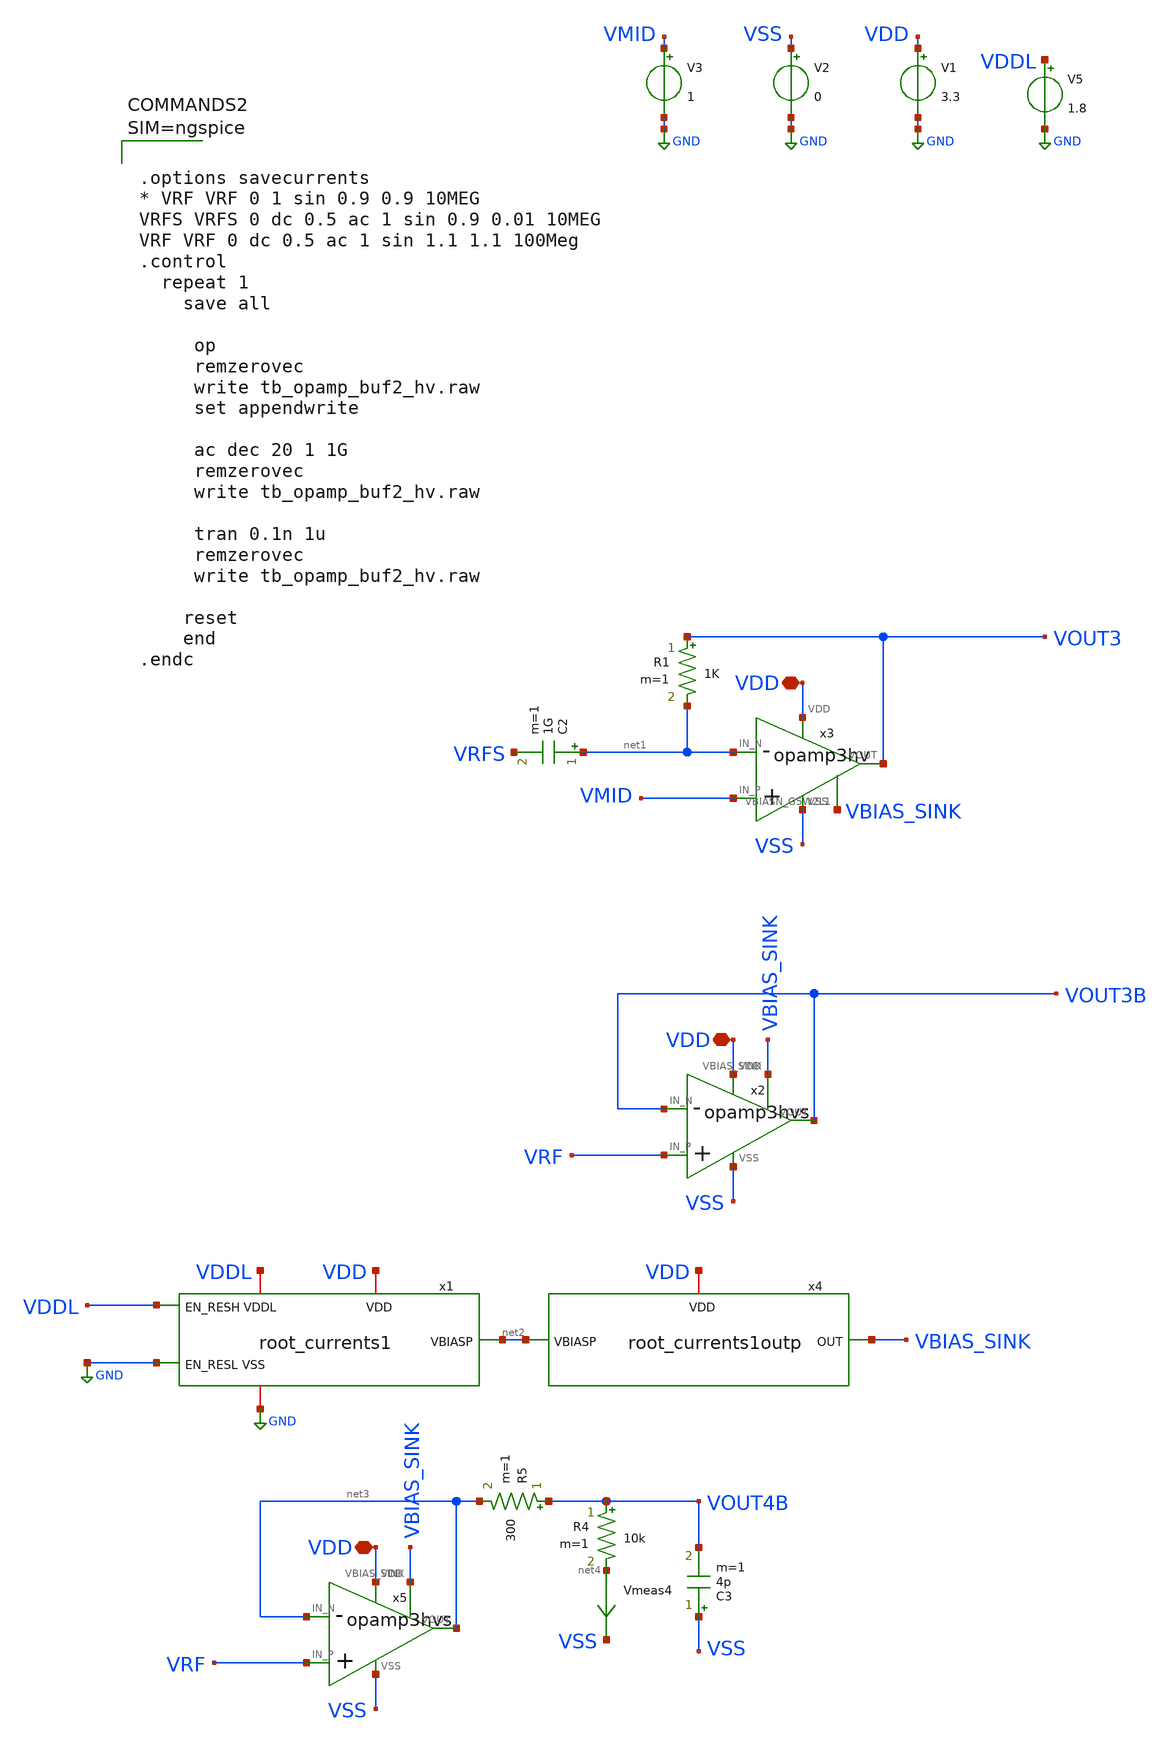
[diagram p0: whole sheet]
** sch_path: xschem/tb_opamp_buf2_hv.sch
**.subckt tb_opamp_buf2_hv VDD VDD VDD
*.iopin VDD
*.iopin VDD
*.iopin VDD
V1 VDD GND 3.3
V2 VSS GND 0
x3 net1 VMID VOUT3 VBIAS_SINK VDD VSS opamp3hv
V3 VMID GND 1
C2 net1 VRFS 1G m=1
R1 VOUT3 net1 1K m=1
x2 VOUT3B VRF VOUT3B VDD VSS VBIAS_SINK opamp3hvs
x1 VDDL GND net2 VDD VDDL GND root_currents1
x4 net2 VBIAS_SINK VDD root_currents1outp
V5 VDDL GND 1.8
x5 net3 VRF net3 VDD VSS VBIAS_SINK opamp3hvs
R4 VOUT4B net4 10k m=1
Vmeas4 net4 VSS 0
.save i(vmeas4)
C3 VSS VOUT4B 4p m=1
R5 VOUT4B net3 300 m=1
**** begin user architecture code

** opencircuitdesign pdks install
.lib $::SKYWATER_MODELS/sky130.lib.spice tt





.options savecurrents
* VRF VRF 0 1 sin 0.9 0.9 10MEG
VRFS VRFS 0 dc 0.5 ac 1 sin 0.9 0.01 10MEG
VRF VRF 0 dc 0.5 ac 1 sin 1.1 1.1 100Meg
.control
  repeat 1
    save all

     op
     remzerovec
     write tb_opamp_buf2_hv.raw
     set appendwrite

     ac dec 20 1 1G
     remzerovec
     write tb_opamp_buf2_hv.raw

     tran 0.1n 1u
     remzerovec
     write tb_opamp_buf2_hv.raw

    reset
    end
.endc



**** end user architecture code
**.ends

* expanding   symbol:  opamp3hv.sym # of pins=6
** sym_path: xschem/opamp3hv.sym
** sch_path: xschem/opamp3hv.sch
.subckt opamp3hv IN_N IN_P VOUT VBIASN_G5W2L1 VDD VSS
*.iopin VDD
*.iopin VSS
*.ipin IN_N
*.opin VOUT
*.ipin IN_P
*.iopin VBIASN_G5W2L1
vimeasn net2 VN 0
.save i(vimeasn)
vimeasp net3 voutstage1 0
.save i(vimeasp)
vicom vcom net1 0
.save i(vicom)
XC1 VOUT voutstage1 sky130_fd_pr__cap_mim_m3_1 W=2 L=2 MF=1 m=1
XM6 net1 VBIASN_G5W2L1 VSS VSS sky130_fd_pr__nfet_g5v0d10v5 L=1 W=2 nf=1 ad='int((nf+1)/2) * W/nf * 0.29'
+ as='int((nf+2)/2) * W/nf * 0.29' pd='2*int((nf+1)/2) * (W/nf + 0.29)' ps='2*int((nf+2)/2) * (W/nf + 0.29)'
+ nrd='0.29 / W' nrs='0.29 / W' sa=0 sb=0 sd=0 mult=1 m=1
XM8 net3 net2 VDD VDD sky130_fd_pr__pfet_g5v0d10v5 L=1 W=2 nf=1 ad='int((nf+1)/2) * W/nf * 0.29' as='int((nf+2)/2) * W/nf * 0.29'
+ pd='2*int((nf+1)/2) * (W/nf + 0.29)' ps='2*int((nf+2)/2) * (W/nf + 0.29)' nrd='0.29 / W' nrs='0.29 / W'
+ sa=0 sb=0 sd=0 mult=1 m=1
XM2 net2 net2 VDD VDD sky130_fd_pr__pfet_g5v0d10v5 L=1 W=2 nf=1 ad='int((nf+1)/2) * W/nf * 0.29' as='int((nf+2)/2) * W/nf * 0.29'
+ pd='2*int((nf+1)/2) * (W/nf + 0.29)' ps='2*int((nf+2)/2) * (W/nf + 0.29)' nrd='0.29 / W' nrs='0.29 / W'
+ sa=0 sb=0 sd=0 mult=1 m=1
XM1 VOUT voutstage1 net4 VDD sky130_fd_pr__pfet_g5v0d10v5 L=0.5 W=16 nf=1 ad='int((nf+1)/2) * W/nf * 0.29'
+ as='int((nf+2)/2) * W/nf * 0.29' pd='2*int((nf+1)/2) * (W/nf + 0.29)' ps='2*int((nf+2)/2) * (W/nf + 0.29)'
+ nrd='0.29 / W' nrs='0.29 / W' sa=0 sb=0 sd=0 mult=2 m=2
XM4 net5 VBIASN_G5W2L1 VSS VSS sky130_fd_pr__nfet_g5v0d10v5 L=0.5 W=8 nf=1 ad='int((nf+1)/2) * W/nf * 0.29'
+ as='int((nf+2)/2) * W/nf * 0.29' pd='2*int((nf+1)/2) * (W/nf + 0.29)' ps='2*int((nf+2)/2) * (W/nf + 0.29)'
+ nrd='0.29 / W' nrs='0.29 / W' sa=0 sb=0 sd=0 mult=2 m=2
XM3 VN IN_N vcom VSS sky130_fd_pr__nfet_03v3_nvt L=0.5 W=4 nf=1 ad='int((nf+1)/2) * W/nf * 0.29' as='int((nf+2)/2) * W/nf * 0.29'
+ pd='2*int((nf+1)/2) * (W/nf + 0.29)' ps='2*int((nf+2)/2) * (W/nf + 0.29)' nrd='0.29 / W' nrs='0.29 / W'
+ sa=0 sb=0 sd=0 mult=4 m=4
XM5 voutstage1 IN_P vcom VSS sky130_fd_pr__nfet_03v3_nvt L=0.5 W=4 nf=1 ad='int((nf+1)/2) * W/nf * 0.29'
+ as='int((nf+2)/2) * W/nf * 0.29' pd='2*int((nf+1)/2) * (W/nf + 0.29)' ps='2*int((nf+2)/2) * (W/nf + 0.29)'
+ nrd='0.29 / W' nrs='0.29 / W' sa=0 sb=0 sd=0 mult=4 m=4
XC2 VDD VSS sky130_fd_pr__cap_mim_m3_1 W=4 L=4 MF=1 m=1
vimeasp1 VDD net4 0
.save i(vimeasp1)
vimeasn1 VOUT net5 0
.save i(vimeasn1)
.ends


* expanding   symbol:  opamp3hvs.sym # of pins=6
** sym_path: xschem/opamp3hvs.sym
** sch_path: xschem/opamp3hvs.sch
.subckt opamp3hvs IN_N IN_P VOUT VDD VSS VBIAS_SINK
*.ipin IN_N
*.ipin IN_P
*.opin VOUT
*.iopin VDD
*.iopin VSS
*.iopin VBIAS_SINK
XM1 net1 net1 VSS VSS sky130_fd_pr__nfet_g5v0d10v5 L=0.5 W=4 nf=1 ad='int((nf+1)/2) * W/nf * 0.29' as='int((nf+2)/2) * W/nf * 0.29'
+ pd='2*int((nf+1)/2) * (W/nf + 0.29)' ps='2*int((nf+2)/2) * (W/nf + 0.29)' nrd='0.29 / W' nrs='0.29 / W'
+ sa=0 sb=0 sd=0 mult=1 m=1
vimeasn2 VBIAS_SINK net1 0
.save i(vimeasn2)
x1 IN_N IN_P VOUT net1 VDD VSS opamp3hv
.ends


* expanding   symbol:  root_currents1.sym # of pins=6
** sym_path: xschem/root_currents1.sym
** sch_path: xschem/root_currents1.sch
.subckt root_currents1 EN_RESH EN_RESL VBIASP VDD VDDL VSS
*.iopin VSS
*.ipin EN_RESH
*.opin VBIASP
*.iopin VDDL
*.iopin VDD
*.ipin EN_RESL
XR1 V1 net2 net4 sky130_fd_pr__res_high_po_0p35 L=20 mult=1 m=1
XR2 V2 net3 net5 sky130_fd_pr__res_high_po_0p69 L=8 mult=1 m=1
XM4 VMID VMID VSS VSS sky130_fd_pr__nfet_01v8_lvt L=0.5 W=4 nf=1 ad='int((nf+1)/2) * W/nf * 0.29' as='int((nf+2)/2) * W/nf * 0.29'
+ pd='2*int((nf+1)/2) * (W/nf + 0.29)' ps='2*int((nf+2)/2) * (W/nf + 0.29)' nrd='0.29 / W' nrs='0.29 / W'
+ sa=0 sb=0 sd=0 mult=1 m=1
XM5 VMID VMID VSS VSS sky130_fd_pr__nfet_01v8_lvt L=0.5 W=4 nf=1 ad='int((nf+1)/2) * W/nf * 0.29' as='int((nf+2)/2) * W/nf * 0.29'
+ pd='2*int((nf+1)/2) * (W/nf + 0.29)' ps='2*int((nf+2)/2) * (W/nf + 0.29)' nrd='0.29 / W' nrs='0.29 / W'
+ sa=0 sb=0 sd=0 mult=1 m=1
XM6 net1 VMID VSS VSS sky130_fd_pr__nfet_01v8_lvt L=0.5 W=4 nf=1 ad='int((nf+1)/2) * W/nf * 0.29' as='int((nf+2)/2) * W/nf * 0.29'
+ pd='2*int((nf+1)/2) * (W/nf + 0.29)' ps='2*int((nf+2)/2) * (W/nf + 0.29)' nrd='0.29 / W' nrs='0.29 / W'
+ sa=0 sb=0 sd=0 mult=1 m=1
XM2 V1 EN_RESH_VDD VMID VSS sky130_fd_pr__nfet_g5v0d10v5 L=0.5 W=4 nf=1 ad='int((nf+1)/2) * W/nf * 0.29'
+ as='int((nf+2)/2) * W/nf * 0.29' pd='2*int((nf+1)/2) * (W/nf + 0.29)' ps='2*int((nf+2)/2) * (W/nf + 0.29)'
+ nrd='0.29 / W' nrs='0.29 / W' sa=0 sb=0 sd=0 mult=1 m=1
viout VBIASP net1 0
.save i(viout)
x1 EN_RESH EN_RESH_VDD net6 VDD VDDL VSS lvl_shift_lohi1
XM7 VBIASP VBIASP VDD VDD sky130_fd_pr__pfet_g5v0d10v5 L=0.5 W=4 nf=1 ad='int((nf+1)/2) * W/nf * 0.29'
+ as='int((nf+2)/2) * W/nf * 0.29' pd='2*int((nf+1)/2) * (W/nf + 0.29)' ps='2*int((nf+2)/2) * (W/nf + 0.29)'
+ nrd='0.29 / W' nrs='0.29 / W' sa=0 sb=0 sd=0 mult=1 m=1
vin1 VDD net2 0
.save i(vin1)
vin2 VDDL net3 0
.save i(vin2)
XM1 V2 EN_RESL VMID VSS sky130_fd_pr__nfet_01v8_lvt L=0.5 W=4 nf=1 ad='int((nf+1)/2) * W/nf * 0.29' as='int((nf+2)/2) * W/nf * 0.29'
+ pd='2*int((nf+1)/2) * (W/nf + 0.29)' ps='2*int((nf+2)/2) * (W/nf + 0.29)' nrd='0.29 / W' nrs='0.29 / W'
+ sa=0 sb=0 sd=0 mult=1 m=1
.ends


* expanding   symbol:  root_currents1outp.sym # of pins=3
** sym_path: xschem/root_currents1outp.sym
** sch_path: xschem/root_currents1outp.sch
.subckt root_currents1outp VBIASP OUT VDD
*.iopin VBIASP
*.iopin OUT
*.iopin VDD
XM7 net1 VBIASP VDD VDD sky130_fd_pr__pfet_g5v0d10v5 L=0.5 W=4 nf=1 ad='int((nf+1)/2) * W/nf * 0.29'
+ as='int((nf+2)/2) * W/nf * 0.29' pd='2*int((nf+1)/2) * (W/nf + 0.29)' ps='2*int((nf+2)/2) * (W/nf + 0.29)'
+ nrd='0.29 / W' nrs='0.29 / W' sa=0 sb=0 sd=0 mult=1 m=1
viout net1 OUT 0
.save i(viout)
.ends


* expanding   symbol:  lvl_shift_lohi1.sym # of pins=6
** sym_path: xschem/lvl_shift_lohi1.sym
** sch_path: xschem/lvl_shift_lohi1.sch
.subckt lvl_shift_lohi1 D Q QB VDDH VDDL VSS
*.ipin D
*.opin Q
*.opin QB
*.iopin VDDH
*.iopin VDDL
*.iopin VSS
vpwr VDDL net1 0
.save i(vpwr)
XM1 QB Q VDDH VDDH sky130_fd_pr__pfet_g5v0d10v5 L=0.5 W=2 nf=1 ad='int((nf+1)/2) * W/nf * 0.29' as='int((nf+2)/2) * W/nf * 0.29'
+ pd='2*int((nf+1)/2) * (W/nf + 0.29)' ps='2*int((nf+2)/2) * (W/nf + 0.29)' nrd='0.29 / W' nrs='0.29 / W'
+ sa=0 sb=0 sd=0 mult=1 m=1
XM2 Q QB VDDH VDDH sky130_fd_pr__pfet_g5v0d10v5 L=0.5 W=2 nf=1 ad='int((nf+1)/2) * W/nf * 0.29' as='int((nf+2)/2) * W/nf * 0.29'
+ pd='2*int((nf+1)/2) * (W/nf + 0.29)' ps='2*int((nf+2)/2) * (W/nf + 0.29)' nrd='0.29 / W' nrs='0.29 / W'
+ sa=0 sb=0 sd=0 mult=1 m=1
XM3 QB D VSS VSS sky130_fd_pr__nfet_g5v0d10v5 L=0.5 W=4 nf=1 ad='int((nf+1)/2) * W/nf * 0.29' as='int((nf+2)/2) * W/nf * 0.29'
+ pd='2*int((nf+1)/2) * (W/nf + 0.29)' ps='2*int((nf+2)/2) * (W/nf + 0.29)' nrd='0.29 / W' nrs='0.29 / W'
+ sa=0 sb=0 sd=0 mult=1 m=1
XM4 Q DB VSS VSS sky130_fd_pr__nfet_g5v0d10v5 L=0.5 W=4 nf=1 ad='int((nf+1)/2) * W/nf * 0.29' as='int((nf+2)/2) * W/nf * 0.29'
+ pd='2*int((nf+1)/2) * (W/nf + 0.29)' ps='2*int((nf+2)/2) * (W/nf + 0.29)' nrd='0.29 / W' nrs='0.29 / W'
+ sa=0 sb=0 sd=0 mult=1 m=1
XM5 DB D VSS VSS sky130_fd_pr__nfet_01v8_lvt L=0.5 W=1 nf=1 ad='int((nf+1)/2) * W/nf * 0.29' as='int((nf+2)/2) * W/nf * 0.29'
+ pd='2*int((nf+1)/2) * (W/nf + 0.29)' ps='2*int((nf+2)/2) * (W/nf + 0.29)' nrd='0.29 / W' nrs='0.29 / W'
+ sa=0 sb=0 sd=0 mult=1 m=1
XM6 DB D net1 VDDL sky130_fd_pr__pfet_01v8_lvt L=0.5 W=2 nf=1 ad='int((nf+1)/2) * W/nf * 0.29' as='int((nf+2)/2) * W/nf * 0.29'
+ pd='2*int((nf+1)/2) * (W/nf + 0.29)' ps='2*int((nf+2)/2) * (W/nf + 0.29)' nrd='0.29 / W' nrs='0.29 / W'
+ sa=0 sb=0 sd=0 mult=1 m=1
.ends

.GLOBAL GND
.end
